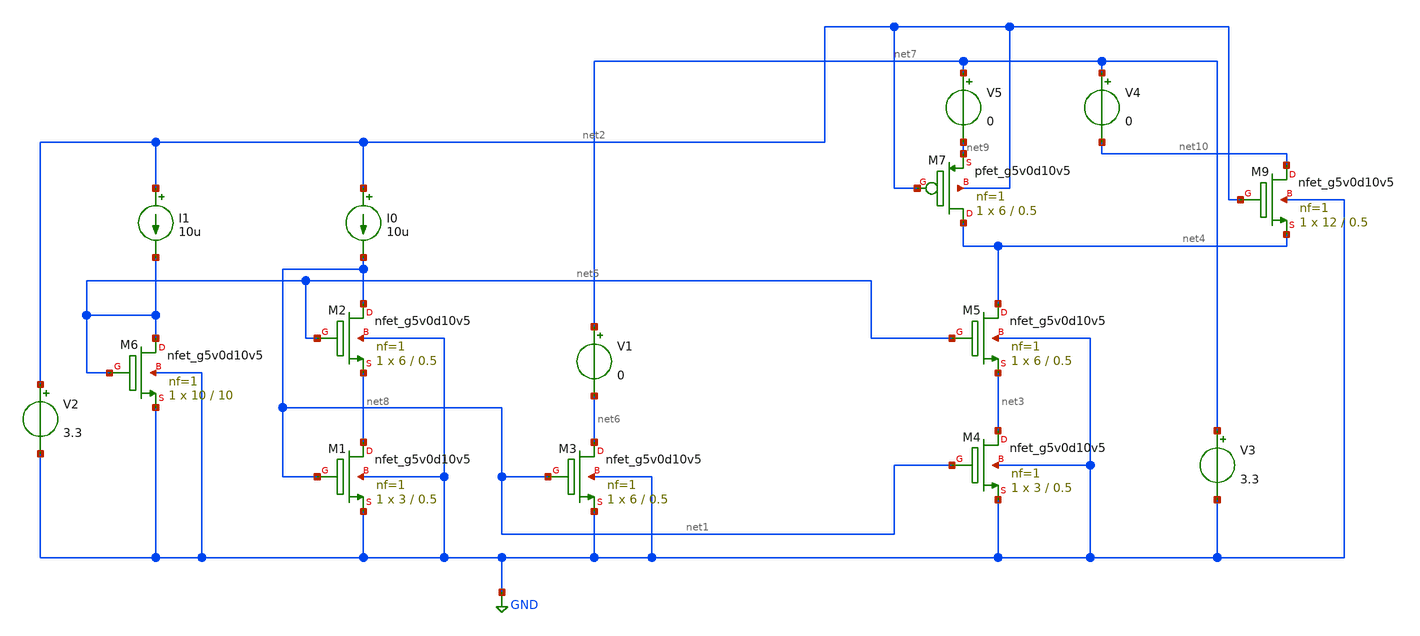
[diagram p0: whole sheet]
** sch_path: xschem/currentmirror_tb.sch
**.subckt currentmirror_tb
I0 net2 net1 10u
V1 net7 net6 0
V2 net2 GND 3.3
XM1 net8 net1 GND GND sky130_fd_pr__nfet_g5v0d10v5 L=0.5 W=3 nf=1 ad='int((nf+1)/2) * W/nf * 0.29' as='int((nf+2)/2) * W/nf * 0.29'
+ pd='2*int((nf+1)/2) * (W/nf + 0.29)' ps='2*int((nf+2)/2) * (W/nf + 0.29)' nrd='0.29 / W' nrs='0.29 / W'
+ sa=0 sb=0 sd=0 mult=1 m=1
XM3 net6 net1 GND GND sky130_fd_pr__nfet_g5v0d10v5 L=0.5 W=6 nf=1 ad='int((nf+1)/2) * W/nf * 0.29' as='int((nf+2)/2) * W/nf * 0.29'
+ pd='2*int((nf+1)/2) * (W/nf + 0.29)' ps='2*int((nf+2)/2) * (W/nf + 0.29)' nrd='0.29 / W' nrs='0.29 / W'
+ sa=0 sb=0 sd=0 mult=1 m=1
XM4 net3 net1 GND GND sky130_fd_pr__nfet_g5v0d10v5 L=0.5 W=3 nf=1 ad='int((nf+1)/2) * W/nf * 0.29' as='int((nf+2)/2) * W/nf * 0.29'
+ pd='2*int((nf+1)/2) * (W/nf + 0.29)' ps='2*int((nf+2)/2) * (W/nf + 0.29)' nrd='0.29 / W' nrs='0.29 / W'
+ sa=0 sb=0 sd=0 mult=1 m=1
XM5 net4 net5 net3 GND sky130_fd_pr__nfet_g5v0d10v5 L=0.5 W=6 nf=1 ad='int((nf+1)/2) * W/nf * 0.29' as='int((nf+2)/2) * W/nf * 0.29'
+ pd='2*int((nf+1)/2) * (W/nf + 0.29)' ps='2*int((nf+2)/2) * (W/nf + 0.29)' nrd='0.29 / W' nrs='0.29 / W'
+ sa=0 sb=0 sd=0 mult=1 m=1
V3 net7 GND 3.3
XM6 net5 net5 GND GND sky130_fd_pr__nfet_g5v0d10v5 L=10 W=10 nf=1 ad='int((nf+1)/2) * W/nf * 0.29' as='int((nf+2)/2) * W/nf * 0.29'
+ pd='2*int((nf+1)/2) * (W/nf + 0.29)' ps='2*int((nf+2)/2) * (W/nf + 0.29)' nrd='0.29 / W' nrs='0.29 / W'
+ sa=0 sb=0 sd=0 mult=1 m=1
V4 net7 net10 0
I1 net2 net5 10u
XM2 net1 net5 net8 GND sky130_fd_pr__nfet_g5v0d10v5 L=0.5 W=6 nf=1 ad='int((nf+1)/2) * W/nf * 0.29' as='int((nf+2)/2) * W/nf * 0.29'
+ pd='2*int((nf+1)/2) * (W/nf + 0.29)' ps='2*int((nf+2)/2) * (W/nf + 0.29)' nrd='0.29 / W' nrs='0.29 / W'
+ sa=0 sb=0 sd=0 mult=1 m=1
V5 net7 net9 0
XM7 net4 net2 net9 net2 sky130_fd_pr__pfet_g5v0d10v5 L=0.5 W=6 nf=1 ad='int((nf+1)/2) * W/nf * 0.29'
+ as='int((nf+2)/2) * W/nf * 0.29' pd='2*int((nf+1)/2) * (W/nf + 0.29)' ps='2*int((nf+2)/2) * (W/nf + 0.29)'
+ nrd='0.29 / W' nrs='0.29 / W' sa=0 sb=0 sd=0 mult=1 m=1
XM9 net10 net2 net4 GND sky130_fd_pr__nfet_g5v0d10v5 L=0.5 W=12 nf=1 ad='int((nf+1)/2) * W/nf * 0.29'
+ as='int((nf+2)/2) * W/nf * 0.29' pd='2*int((nf+1)/2) * (W/nf + 0.29)' ps='2*int((nf+2)/2) * (W/nf + 0.29)'
+ nrd='0.29 / W' nrs='0.29 / W' sa=0 sb=0 sd=0 mult=1 m=1
**** begin user architecture code
 .lib $::SKYWATER_MODELS/sky130.lib.spice tt

.param mc_mm_switch=0
.param mc_pr_switch=1



.option wnflag=0
.option savecurrents
.control
save all
dc v3 0 3.3 0.01
plot i(V1) i(V4)
write currentmirrortb.raw
op
.endc


**** end user architecture code
**.ends
.GLOBAL GND
.end
